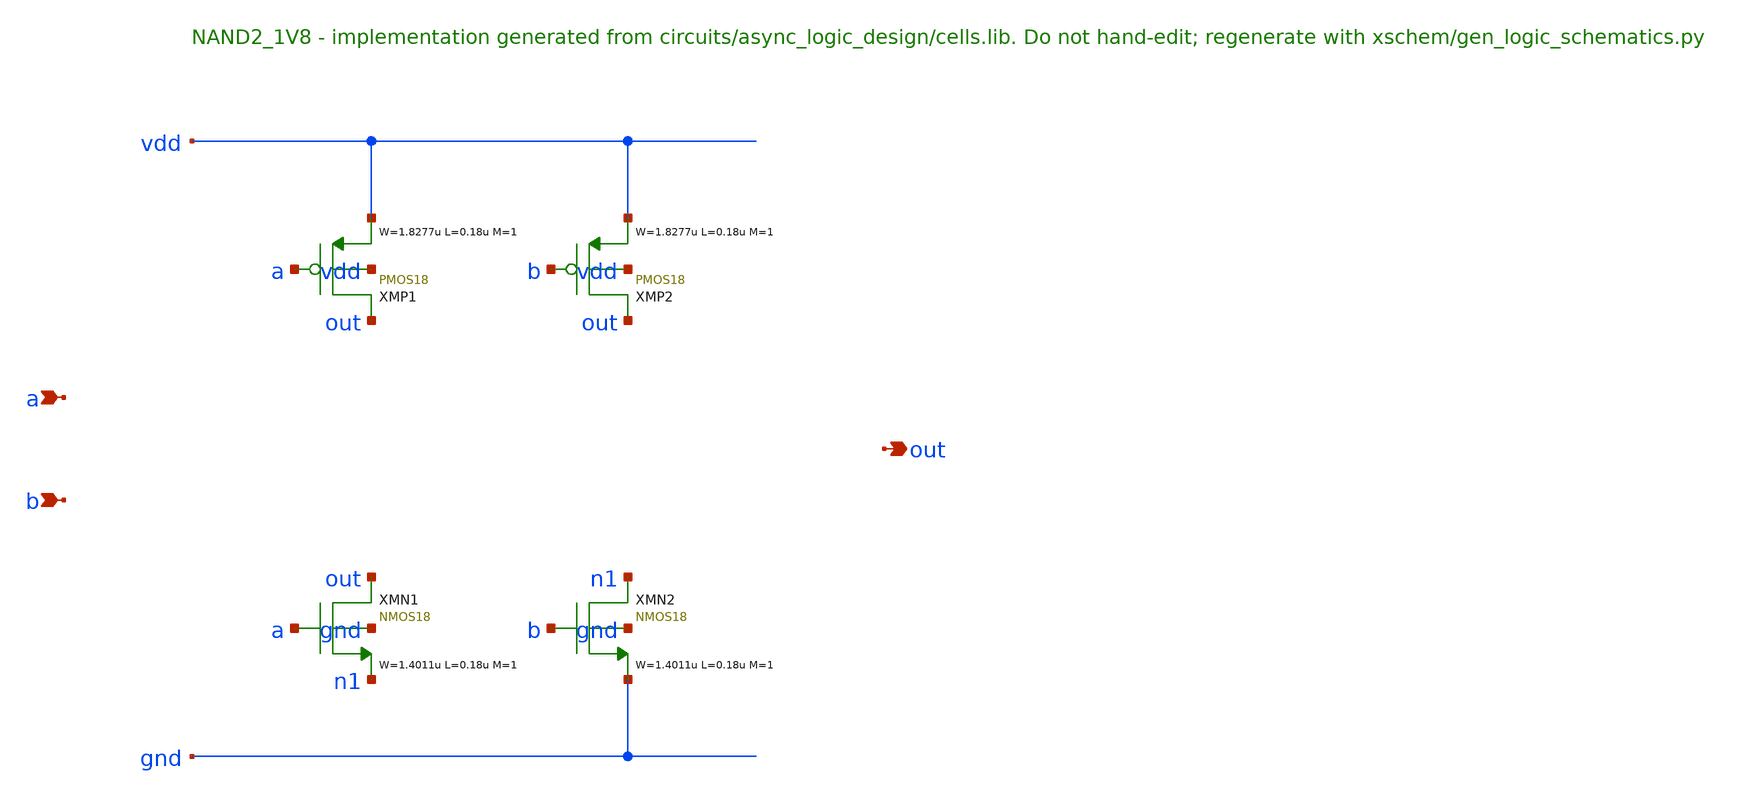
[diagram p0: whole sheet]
** sch_path: xschem/logic/NAND2_1V8.sch
**.subckt NAND2_1V8 a b out
*.ipin a
*.ipin b
*.opin out
XMP1 out a vdd vdd PMOS18 W=1.8277u L=0.18u M=1 MM_SIGMA=0
XMP2 out b vdd vdd PMOS18 W=1.8277u L=0.18u M=1 MM_SIGMA=0
XMN1 out a n1 gnd NMOS18 W=1.4011u L=0.18u M=1 MM_SIGMA=0
XMN2 n1 b gnd gnd NMOS18 W=1.4011u L=0.18u M=1 MM_SIGMA=0
**.ends
.end
